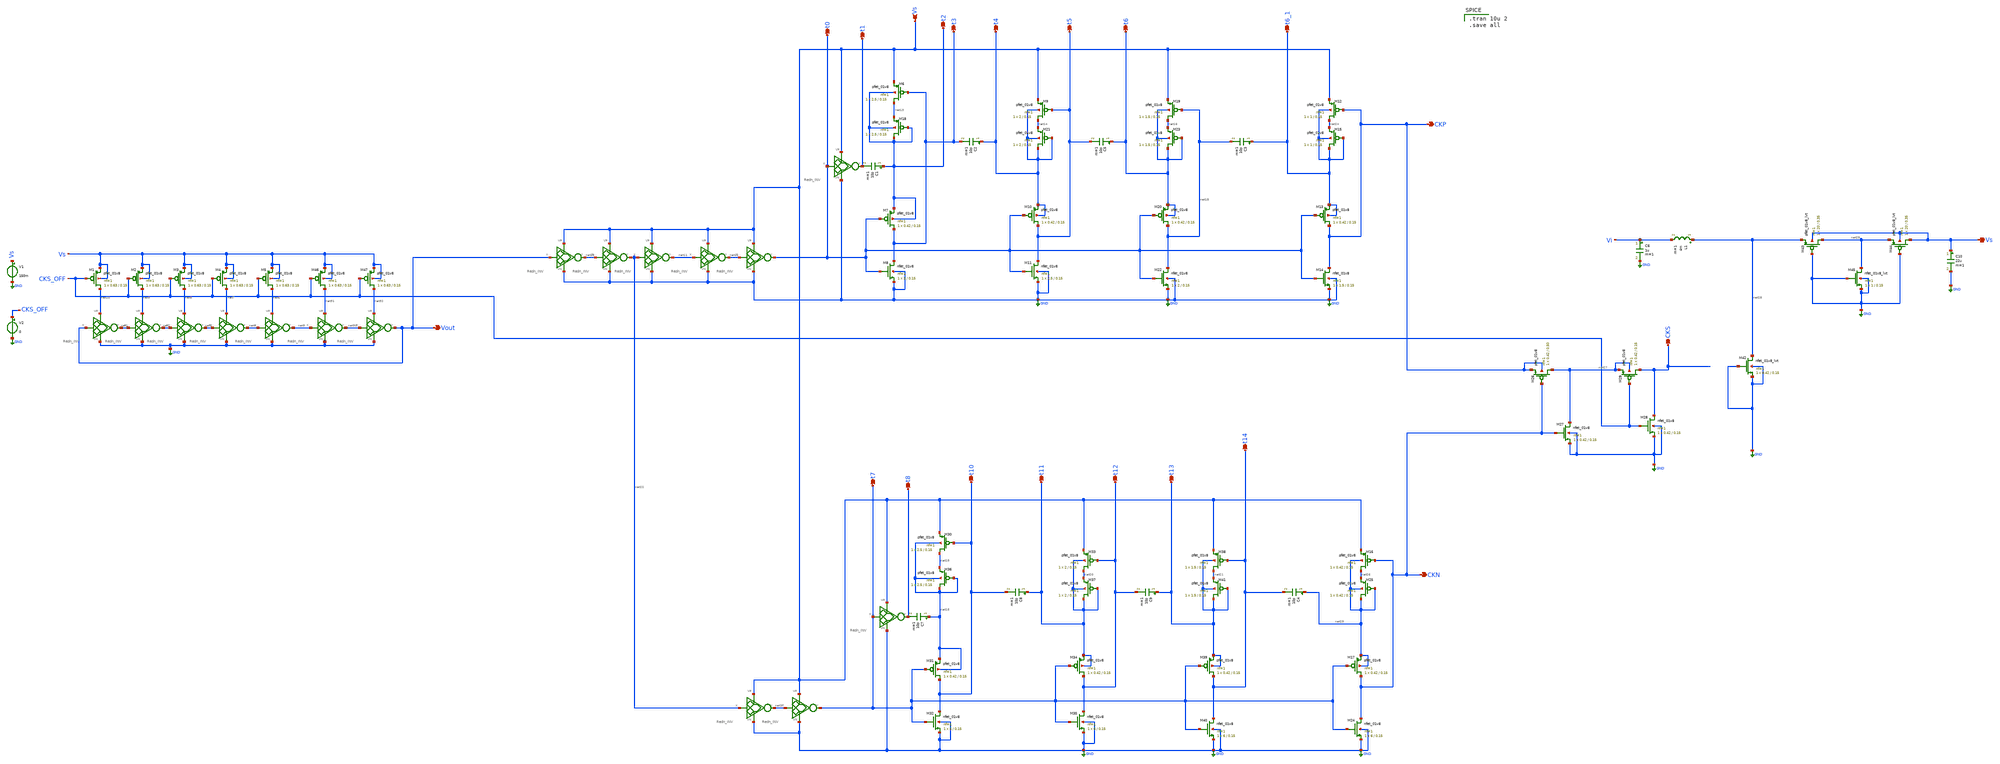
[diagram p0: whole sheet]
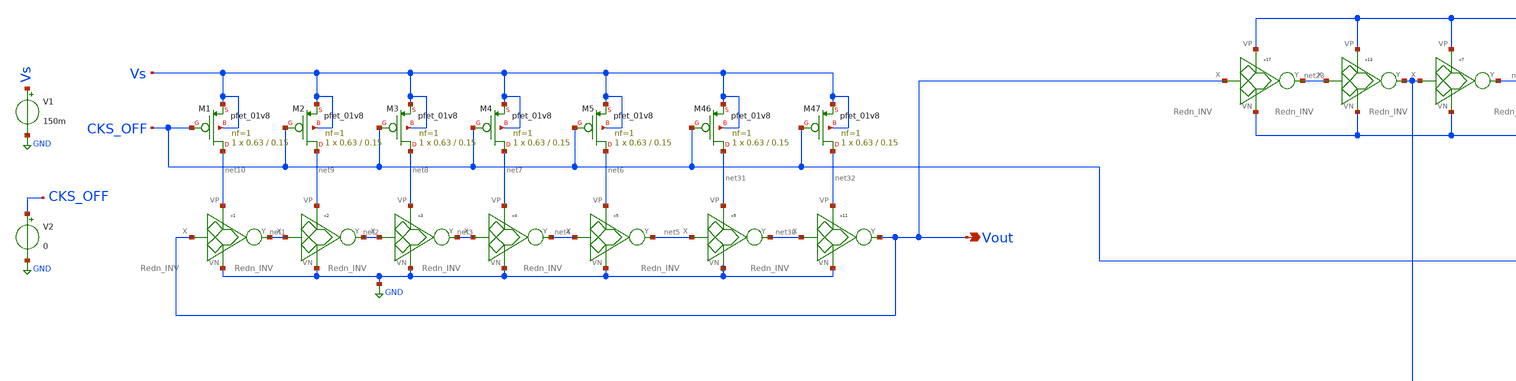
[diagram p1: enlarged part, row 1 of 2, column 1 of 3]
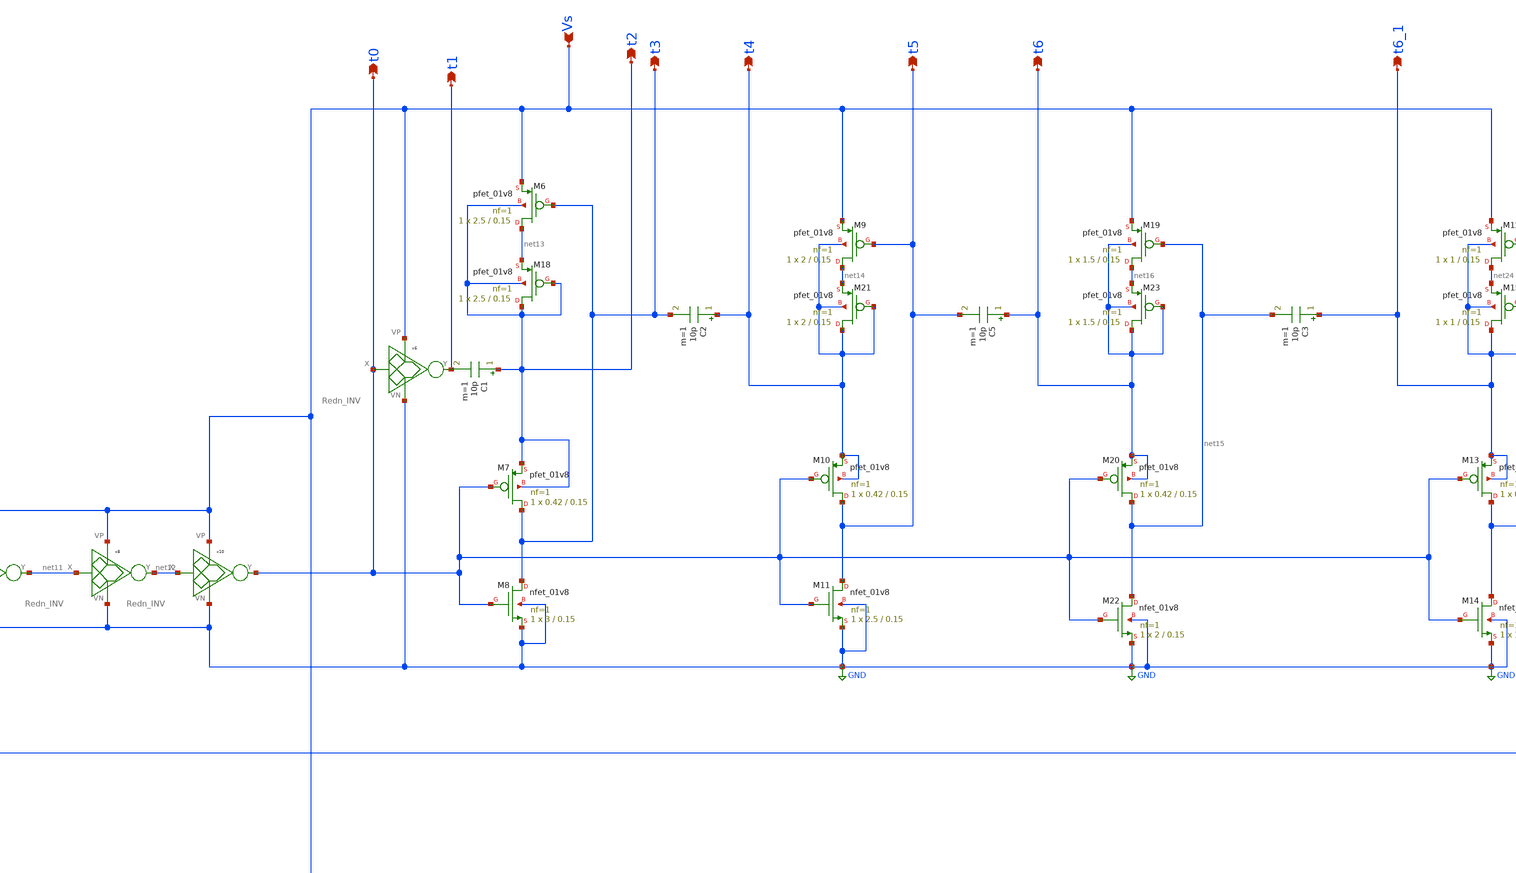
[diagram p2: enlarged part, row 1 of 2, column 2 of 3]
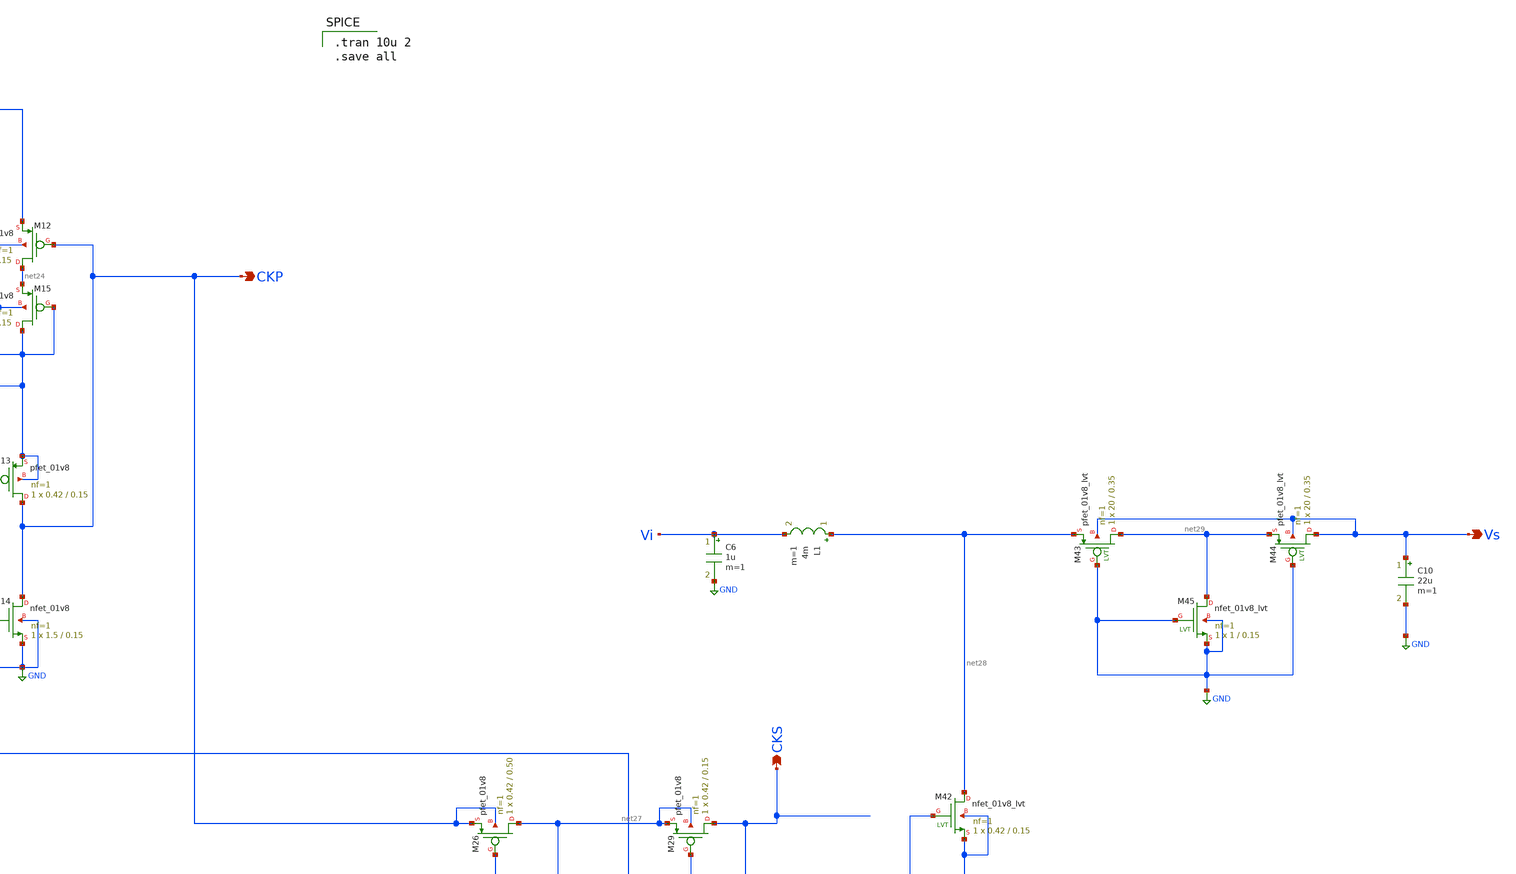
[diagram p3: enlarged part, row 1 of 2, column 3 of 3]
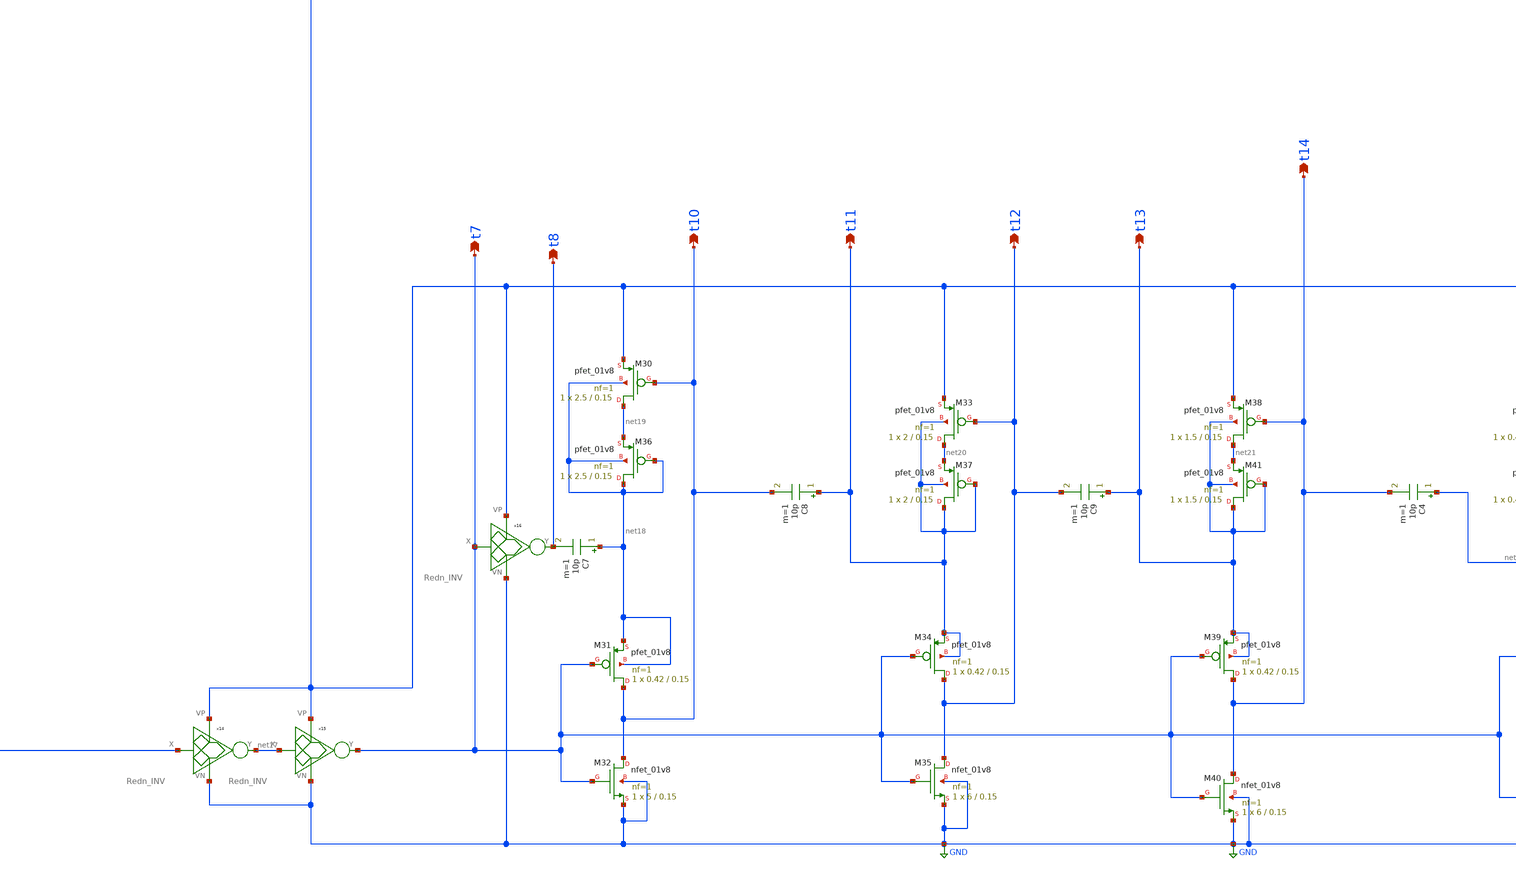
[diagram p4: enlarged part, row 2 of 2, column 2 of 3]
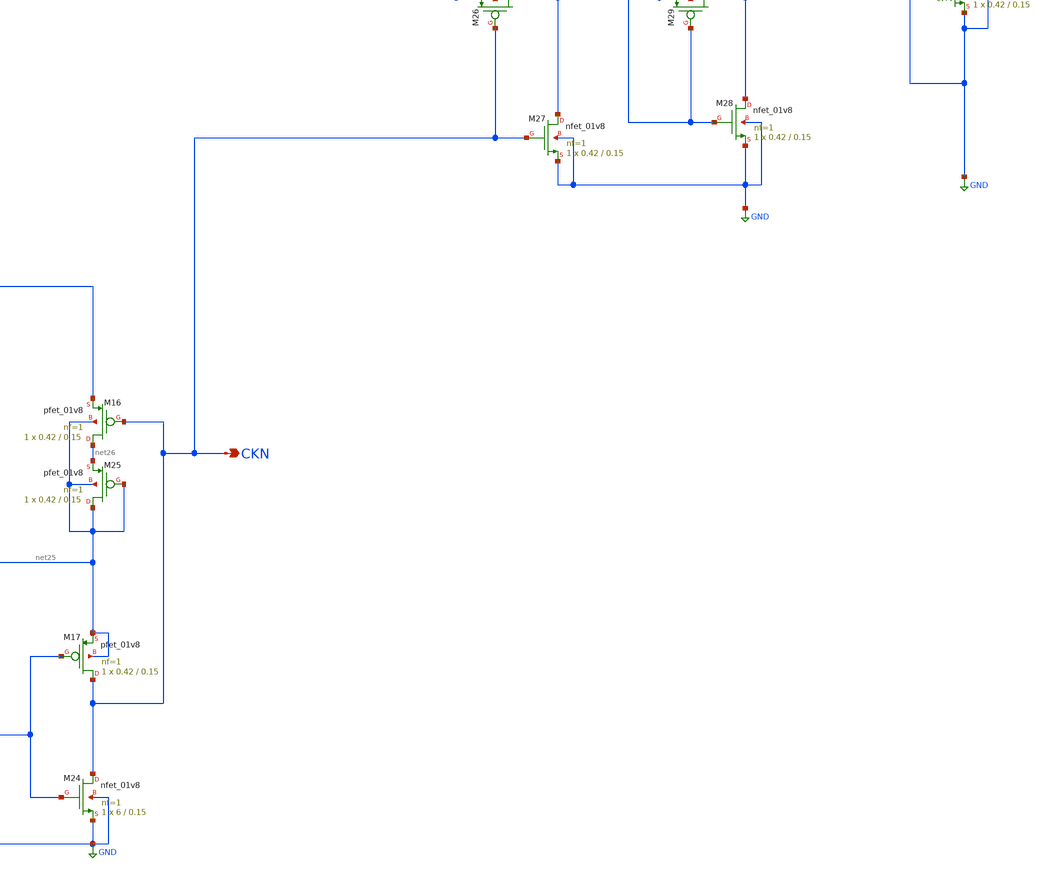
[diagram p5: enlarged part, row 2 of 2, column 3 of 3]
** sch_path: Blocks/Startup Converter/Startup_Cnv_2.sch
**.subckt Startup_Cnv_2 Vout Vs t2 t3 t4 t1 t0 t6 t5 t10 t11 t8 t7 t13 t12 CKP t6_1 CKN t14 CKS Vs
*.opin Vout
*.ipin Vs
*.opin t2
*.opin t3
*.opin t4
*.opin t1
*.opin t0
*.opin t6
*.opin t5
*.opin t10
*.opin t11
*.opin t8
*.opin t7
*.opin t13
*.opin t12
*.opin CKP
*.opin t6_1
*.opin CKN
*.opin t14
*.opin CKS
*.opin Vs
V1 Vs GND 150m
XM1 net10 CKS_OFF Vs Vs sky130_fd_pr__pfet_01v8 L=0.15 W=0.63 nf=1 ad='int((nf+1)/2) * W/nf * 0.29' as='int((nf+2)/2) * W/nf * 0.29'
+ pd='2*int((nf+1)/2) * (W/nf + 0.29)' ps='2*int((nf+2)/2) * (W/nf + 0.29)' nrd='0.29 / W' nrs='0.29 / W'
+ sa=0 sb=0 sd=0 mult=1 m=1
XM2 net9 CKS_OFF Vs Vs sky130_fd_pr__pfet_01v8 L=0.15 W=0.63 nf=1 ad='int((nf+1)/2) * W/nf * 0.29' as='int((nf+2)/2) * W/nf * 0.29'
+ pd='2*int((nf+1)/2) * (W/nf + 0.29)' ps='2*int((nf+2)/2) * (W/nf + 0.29)' nrd='0.29 / W' nrs='0.29 / W'
+ sa=0 sb=0 sd=0 mult=1 m=1
XM3 net8 CKS_OFF Vs Vs sky130_fd_pr__pfet_01v8 L=0.15 W=0.63 nf=1 ad='int((nf+1)/2) * W/nf * 0.29' as='int((nf+2)/2) * W/nf * 0.29'
+ pd='2*int((nf+1)/2) * (W/nf + 0.29)' ps='2*int((nf+2)/2) * (W/nf + 0.29)' nrd='0.29 / W' nrs='0.29 / W'
+ sa=0 sb=0 sd=0 mult=1 m=1
XM4 net7 CKS_OFF Vs Vs sky130_fd_pr__pfet_01v8 L=0.15 W=0.63 nf=1 ad='int((nf+1)/2) * W/nf * 0.29' as='int((nf+2)/2) * W/nf * 0.29'
+ pd='2*int((nf+1)/2) * (W/nf + 0.29)' ps='2*int((nf+2)/2) * (W/nf + 0.29)' nrd='0.29 / W' nrs='0.29 / W'
+ sa=0 sb=0 sd=0 mult=1 m=1
XM5 net6 CKS_OFF Vs Vs sky130_fd_pr__pfet_01v8 L=0.15 W=0.63 nf=1 ad='int((nf+1)/2) * W/nf * 0.29' as='int((nf+2)/2) * W/nf * 0.29'
+ pd='2*int((nf+1)/2) * (W/nf + 0.29)' ps='2*int((nf+2)/2) * (W/nf + 0.29)' nrd='0.29 / W' nrs='0.29 / W'
+ sa=0 sb=0 sd=0 mult=1 m=1
V2 CKS_OFF GND 0
x1 Vout net1 net10 GND Redn_INV
x2 net1 net2 net9 GND Redn_INV
x3 net2 net3 net8 GND Redn_INV
x4 net3 net4 net7 GND Redn_INV
x5 net4 net5 net6 GND Redn_INV
C1 t2 t1 10p m=1
XM6 net13 t3 Vs t2 sky130_fd_pr__pfet_01v8 L=0.15 W=2.5 nf=1 ad='int((nf+1)/2) * W/nf * 0.29' as='int((nf+2)/2) * W/nf * 0.29'
+ pd='2*int((nf+1)/2) * (W/nf + 0.29)' ps='2*int((nf+2)/2) * (W/nf + 0.29)' nrd='0.29 / W' nrs='0.29 / W'
+ sa=0 sb=0 sd=0 mult=1 m=1
XM7 t3 t0 t2 t2 sky130_fd_pr__pfet_01v8 L=0.15 W=0.42 nf=1 ad='int((nf+1)/2) * W/nf * 0.29' as='int((nf+2)/2) * W/nf * 0.29'
+ pd='2*int((nf+1)/2) * (W/nf + 0.29)' ps='2*int((nf+2)/2) * (W/nf + 0.29)' nrd='0.29 / W' nrs='0.29 / W'
+ sa=0 sb=0 sd=0 mult=1 m=1
XM8 t3 t0 GND GND sky130_fd_pr__nfet_01v8 L=0.15 W=3 nf=1 ad='int((nf+1)/2) * W/nf * 0.29' as='int((nf+2)/2) * W/nf * 0.29'
+ pd='2*int((nf+1)/2) * (W/nf + 0.29)' ps='2*int((nf+2)/2) * (W/nf + 0.29)' nrd='0.29 / W' nrs='0.29 / W'
+ sa=0 sb=0 sd=0 mult=1 m=1
XM9 net14 t5 Vs t4 sky130_fd_pr__pfet_01v8 L=0.15 W=2 nf=1 ad='int((nf+1)/2) * W/nf * 0.29' as='int((nf+2)/2) * W/nf * 0.29'
+ pd='2*int((nf+1)/2) * (W/nf + 0.29)' ps='2*int((nf+2)/2) * (W/nf + 0.29)' nrd='0.29 / W' nrs='0.29 / W'
+ sa=0 sb=0 sd=0 mult=1 m=1
XM10 t5 t0 t4 t4 sky130_fd_pr__pfet_01v8 L=0.15 W=0.42 nf=1 ad='int((nf+1)/2) * W/nf * 0.29' as='int((nf+2)/2) * W/nf * 0.29'
+ pd='2*int((nf+1)/2) * (W/nf + 0.29)' ps='2*int((nf+2)/2) * (W/nf + 0.29)' nrd='0.29 / W' nrs='0.29 / W'
+ sa=0 sb=0 sd=0 mult=1 m=1
XM11 t5 t0 GND GND sky130_fd_pr__nfet_01v8 L=0.15 W=2.5 nf=1 ad='int((nf+1)/2) * W/nf * 0.29' as='int((nf+2)/2) * W/nf * 0.29'
+ pd='2*int((nf+1)/2) * (W/nf + 0.29)' ps='2*int((nf+2)/2) * (W/nf + 0.29)' nrd='0.29 / W' nrs='0.29 / W'
+ sa=0 sb=0 sd=0 mult=1 m=1
XM18 t2 t2 net13 t2 sky130_fd_pr__pfet_01v8 L=0.15 W=2.5 nf=1 ad='int((nf+1)/2) * W/nf * 0.29' as='int((nf+2)/2) * W/nf * 0.29'
+ pd='2*int((nf+1)/2) * (W/nf + 0.29)' ps='2*int((nf+2)/2) * (W/nf + 0.29)' nrd='0.29 / W' nrs='0.29 / W'
+ sa=0 sb=0 sd=0 mult=1 m=1
XM21 t4 t4 net14 t4 sky130_fd_pr__pfet_01v8 L=0.15 W=2 nf=1 ad='int((nf+1)/2) * W/nf * 0.29' as='int((nf+2)/2) * W/nf * 0.29'
+ pd='2*int((nf+1)/2) * (W/nf + 0.29)' ps='2*int((nf+2)/2) * (W/nf + 0.29)' nrd='0.29 / W' nrs='0.29 / W'
+ sa=0 sb=0 sd=0 mult=1 m=1
C2 t4 t3 10p m=1
x7 net22 net11 Vs GND Redn_INV
x8 net11 net12 Vs GND Redn_INV
x10 net12 t0 Vs GND Redn_INV
x6 t0 t1 Vs GND Redn_INV
XM19 net16 net15 Vs t6 sky130_fd_pr__pfet_01v8 L=0.15 W=1.5 nf=1 ad='int((nf+1)/2) * W/nf * 0.29' as='int((nf+2)/2) * W/nf * 0.29'
+ pd='2*int((nf+1)/2) * (W/nf + 0.29)' ps='2*int((nf+2)/2) * (W/nf + 0.29)' nrd='0.29 / W' nrs='0.29 / W'
+ sa=0 sb=0 sd=0 mult=1 m=1
XM20 net15 t0 t6 t6 sky130_fd_pr__pfet_01v8 L=0.15 W=0.42 nf=1 ad='int((nf+1)/2) * W/nf * 0.29' as='int((nf+2)/2) * W/nf * 0.29'
+ pd='2*int((nf+1)/2) * (W/nf + 0.29)' ps='2*int((nf+2)/2) * (W/nf + 0.29)' nrd='0.29 / W' nrs='0.29 / W'
+ sa=0 sb=0 sd=0 mult=1 m=1
XM22 net15 t0 GND GND sky130_fd_pr__nfet_01v8 L=0.15 W=2 nf=1 ad='int((nf+1)/2) * W/nf * 0.29' as='int((nf+2)/2) * W/nf * 0.29'
+ pd='2*int((nf+1)/2) * (W/nf + 0.29)' ps='2*int((nf+2)/2) * (W/nf + 0.29)' nrd='0.29 / W' nrs='0.29 / W'
+ sa=0 sb=0 sd=0 mult=1 m=1
XM23 t6 t6 net16 t6 sky130_fd_pr__pfet_01v8 L=0.15 W=1.5 nf=1 ad='int((nf+1)/2) * W/nf * 0.29' as='int((nf+2)/2) * W/nf * 0.29'
+ pd='2*int((nf+1)/2) * (W/nf + 0.29)' ps='2*int((nf+2)/2) * (W/nf + 0.29)' nrd='0.29 / W' nrs='0.29 / W'
+ sa=0 sb=0 sd=0 mult=1 m=1
C5 t6 t5 10p m=1
C7 net18 t8 10p m=1
XM30 net19 t10 Vs net18 sky130_fd_pr__pfet_01v8 L=0.15 W=2.5 nf=1 ad='int((nf+1)/2) * W/nf * 0.29' as='int((nf+2)/2) * W/nf * 0.29'
+ pd='2*int((nf+1)/2) * (W/nf + 0.29)' ps='2*int((nf+2)/2) * (W/nf + 0.29)' nrd='0.29 / W' nrs='0.29 / W'
+ sa=0 sb=0 sd=0 mult=1 m=1
XM31 t10 t7 net18 net18 sky130_fd_pr__pfet_01v8 L=0.15 W=0.42 nf=1 ad='int((nf+1)/2) * W/nf * 0.29' as='int((nf+2)/2) * W/nf * 0.29'
+ pd='2*int((nf+1)/2) * (W/nf + 0.29)' ps='2*int((nf+2)/2) * (W/nf + 0.29)' nrd='0.29 / W' nrs='0.29 / W'
+ sa=0 sb=0 sd=0 mult=1 m=1
XM32 t10 t7 GND GND sky130_fd_pr__nfet_01v8 L=0.15 W=5 nf=1 ad='int((nf+1)/2) * W/nf * 0.29' as='int((nf+2)/2) * W/nf * 0.29'
+ pd='2*int((nf+1)/2) * (W/nf + 0.29)' ps='2*int((nf+2)/2) * (W/nf + 0.29)' nrd='0.29 / W' nrs='0.29 / W'
+ sa=0 sb=0 sd=0 mult=1 m=1
XM33 net20 t12 Vs t11 sky130_fd_pr__pfet_01v8 L=0.15 W=2 nf=1 ad='int((nf+1)/2) * W/nf * 0.29' as='int((nf+2)/2) * W/nf * 0.29'
+ pd='2*int((nf+1)/2) * (W/nf + 0.29)' ps='2*int((nf+2)/2) * (W/nf + 0.29)' nrd='0.29 / W' nrs='0.29 / W'
+ sa=0 sb=0 sd=0 mult=1 m=1
XM34 t12 t7 t11 t11 sky130_fd_pr__pfet_01v8 L=0.15 W=0.42 nf=1 ad='int((nf+1)/2) * W/nf * 0.29' as='int((nf+2)/2) * W/nf * 0.29'
+ pd='2*int((nf+1)/2) * (W/nf + 0.29)' ps='2*int((nf+2)/2) * (W/nf + 0.29)' nrd='0.29 / W' nrs='0.29 / W'
+ sa=0 sb=0 sd=0 mult=1 m=1
XM35 t12 t7 GND GND sky130_fd_pr__nfet_01v8 L=0.15 W=6 nf=1 ad='int((nf+1)/2) * W/nf * 0.29' as='int((nf+2)/2) * W/nf * 0.29'
+ pd='2*int((nf+1)/2) * (W/nf + 0.29)' ps='2*int((nf+2)/2) * (W/nf + 0.29)' nrd='0.29 / W' nrs='0.29 / W'
+ sa=0 sb=0 sd=0 mult=1 m=1
XM36 net18 net18 net19 net18 sky130_fd_pr__pfet_01v8 L=0.15 W=2.5 nf=1 ad='int((nf+1)/2) * W/nf * 0.29'
+ as='int((nf+2)/2) * W/nf * 0.29' pd='2*int((nf+1)/2) * (W/nf + 0.29)' ps='2*int((nf+2)/2) * (W/nf + 0.29)'
+ nrd='0.29 / W' nrs='0.29 / W' sa=0 sb=0 sd=0 mult=1 m=1
XM37 t11 t11 net20 t11 sky130_fd_pr__pfet_01v8 L=0.15 W=2 nf=1 ad='int((nf+1)/2) * W/nf * 0.29' as='int((nf+2)/2) * W/nf * 0.29'
+ pd='2*int((nf+1)/2) * (W/nf + 0.29)' ps='2*int((nf+2)/2) * (W/nf + 0.29)' nrd='0.29 / W' nrs='0.29 / W'
+ sa=0 sb=0 sd=0 mult=1 m=1
C8 t11 t10 10p m=1
x14 net22 net17 Vs GND Redn_INV
x15 net17 t7 Vs GND Redn_INV
x16 t7 t8 Vs GND Redn_INV
XM38 net21 t14 Vs t13 sky130_fd_pr__pfet_01v8 L=0.15 W=1.5 nf=1 ad='int((nf+1)/2) * W/nf * 0.29' as='int((nf+2)/2) * W/nf * 0.29'
+ pd='2*int((nf+1)/2) * (W/nf + 0.29)' ps='2*int((nf+2)/2) * (W/nf + 0.29)' nrd='0.29 / W' nrs='0.29 / W'
+ sa=0 sb=0 sd=0 mult=1 m=1
XM39 t14 t7 t13 t13 sky130_fd_pr__pfet_01v8 L=0.15 W=0.42 nf=1 ad='int((nf+1)/2) * W/nf * 0.29' as='int((nf+2)/2) * W/nf * 0.29'
+ pd='2*int((nf+1)/2) * (W/nf + 0.29)' ps='2*int((nf+2)/2) * (W/nf + 0.29)' nrd='0.29 / W' nrs='0.29 / W'
+ sa=0 sb=0 sd=0 mult=1 m=1
XM40 t14 t7 GND GND sky130_fd_pr__nfet_01v8 L=0.15 W=6 nf=1 ad='int((nf+1)/2) * W/nf * 0.29' as='int((nf+2)/2) * W/nf * 0.29'
+ pd='2*int((nf+1)/2) * (W/nf + 0.29)' ps='2*int((nf+2)/2) * (W/nf + 0.29)' nrd='0.29 / W' nrs='0.29 / W'
+ sa=0 sb=0 sd=0 mult=1 m=1
XM41 t13 t13 net21 t13 sky130_fd_pr__pfet_01v8 L=0.15 W=1.5 nf=1 ad='int((nf+1)/2) * W/nf * 0.29' as='int((nf+2)/2) * W/nf * 0.29'
+ pd='2*int((nf+1)/2) * (W/nf + 0.29)' ps='2*int((nf+2)/2) * (W/nf + 0.29)' nrd='0.29 / W' nrs='0.29 / W'
+ sa=0 sb=0 sd=0 mult=1 m=1
C9 t13 t12 10p m=1
x13 net23 net22 Vs GND Redn_INV
x17 Vout net23 Vs GND Redn_INV
XM12 net24 CKP Vs t6_1 sky130_fd_pr__pfet_01v8 L=0.15 W=1 nf=1 ad='int((nf+1)/2) * W/nf * 0.29' as='int((nf+2)/2) * W/nf * 0.29'
+ pd='2*int((nf+1)/2) * (W/nf + 0.29)' ps='2*int((nf+2)/2) * (W/nf + 0.29)' nrd='0.29 / W' nrs='0.29 / W'
+ sa=0 sb=0 sd=0 mult=1 m=1
XM13 CKP t0 t6_1 t6_1 sky130_fd_pr__pfet_01v8 L=0.15 W=0.42 nf=1 ad='int((nf+1)/2) * W/nf * 0.29' as='int((nf+2)/2) * W/nf * 0.29'
+ pd='2*int((nf+1)/2) * (W/nf + 0.29)' ps='2*int((nf+2)/2) * (W/nf + 0.29)' nrd='0.29 / W' nrs='0.29 / W'
+ sa=0 sb=0 sd=0 mult=1 m=1
XM14 CKP t0 GND GND sky130_fd_pr__nfet_01v8 L=0.15 W=1.5 nf=1 ad='int((nf+1)/2) * W/nf * 0.29' as='int((nf+2)/2) * W/nf * 0.29'
+ pd='2*int((nf+1)/2) * (W/nf + 0.29)' ps='2*int((nf+2)/2) * (W/nf + 0.29)' nrd='0.29 / W' nrs='0.29 / W'
+ sa=0 sb=0 sd=0 mult=1 m=1
XM15 t6_1 t6_1 net24 t6_1 sky130_fd_pr__pfet_01v8 L=0.15 W=1 nf=1 ad='int((nf+1)/2) * W/nf * 0.29' as='int((nf+2)/2) * W/nf * 0.29'
+ pd='2*int((nf+1)/2) * (W/nf + 0.29)' ps='2*int((nf+2)/2) * (W/nf + 0.29)' nrd='0.29 / W' nrs='0.29 / W'
+ sa=0 sb=0 sd=0 mult=1 m=1
C3 t6_1 net15 10p m=1
XM16 net26 CKN Vs net25 sky130_fd_pr__pfet_01v8 L=0.15 W=0.42 nf=1 ad='int((nf+1)/2) * W/nf * 0.29' as='int((nf+2)/2) * W/nf * 0.29'
+ pd='2*int((nf+1)/2) * (W/nf + 0.29)' ps='2*int((nf+2)/2) * (W/nf + 0.29)' nrd='0.29 / W' nrs='0.29 / W'
+ sa=0 sb=0 sd=0 mult=1 m=1
XM17 CKN t7 net25 net25 sky130_fd_pr__pfet_01v8 L=0.15 W=0.42 nf=1 ad='int((nf+1)/2) * W/nf * 0.29' as='int((nf+2)/2) * W/nf * 0.29'
+ pd='2*int((nf+1)/2) * (W/nf + 0.29)' ps='2*int((nf+2)/2) * (W/nf + 0.29)' nrd='0.29 / W' nrs='0.29 / W'
+ sa=0 sb=0 sd=0 mult=1 m=1
XM24 CKN t7 GND GND sky130_fd_pr__nfet_01v8 L=0.15 W=6 nf=1 ad='int((nf+1)/2) * W/nf * 0.29' as='int((nf+2)/2) * W/nf * 0.29'
+ pd='2*int((nf+1)/2) * (W/nf + 0.29)' ps='2*int((nf+2)/2) * (W/nf + 0.29)' nrd='0.29 / W' nrs='0.29 / W'
+ sa=0 sb=0 sd=0 mult=1 m=1
XM25 net25 net25 net26 net25 sky130_fd_pr__pfet_01v8 L=0.15 W=0.42 nf=1 ad='int((nf+1)/2) * W/nf * 0.29'
+ as='int((nf+2)/2) * W/nf * 0.29' pd='2*int((nf+1)/2) * (W/nf + 0.29)' ps='2*int((nf+2)/2) * (W/nf + 0.29)'
+ nrd='0.29 / W' nrs='0.29 / W' sa=0 sb=0 sd=0 mult=1 m=1
C4 net25 t14 10p m=1
XM26 net27 CKN CKP CKP sky130_fd_pr__pfet_01v8 L=0.50 W=0.42 nf=1 ad='int((nf+1)/2) * W/nf * 0.29' as='int((nf+2)/2) * W/nf * 0.29'
+ pd='2*int((nf+1)/2) * (W/nf + 0.29)' ps='2*int((nf+2)/2) * (W/nf + 0.29)' nrd='0.29 / W' nrs='0.29 / W'
+ sa=0 sb=0 sd=0 mult=1 m=1
XM27 net27 CKN GND GND sky130_fd_pr__nfet_01v8 L=0.15 W=0.42 nf=1 ad='int((nf+1)/2) * W/nf * 0.29' as='int((nf+2)/2) * W/nf * 0.29'
+ pd='2*int((nf+1)/2) * (W/nf + 0.29)' ps='2*int((nf+2)/2) * (W/nf + 0.29)' nrd='0.29 / W' nrs='0.29 / W'
+ sa=0 sb=0 sd=0 mult=1 m=1
XM28 CKS CKS_OFF GND GND sky130_fd_pr__nfet_01v8 L=0.15 W=0.42 nf=1 ad='int((nf+1)/2) * W/nf * 0.29'
+ as='int((nf+2)/2) * W/nf * 0.29' pd='2*int((nf+1)/2) * (W/nf + 0.29)' ps='2*int((nf+2)/2) * (W/nf + 0.29)'
+ nrd='0.29 / W' nrs='0.29 / W' sa=0 sb=0 sd=0 mult=1 m=1
XM29 CKS CKS_OFF net27 net27 sky130_fd_pr__pfet_01v8 L=0.15 W=0.42 nf=1 ad='int((nf+1)/2) * W/nf * 0.29'
+ as='int((nf+2)/2) * W/nf * 0.29' pd='2*int((nf+1)/2) * (W/nf + 0.29)' ps='2*int((nf+2)/2) * (W/nf + 0.29)'
+ nrd='0.29 / W' nrs='0.29 / W' sa=0 sb=0 sd=0 mult=1 m=1
C6 Vi GND 1u m=1
L1 net28 Vi 4m m=1
C10 Vs GND 22u m=1
XM42 net28 GND GND GND sky130_fd_pr__nfet_01v8_lvt L=0.15 W=0.42 nf=1 ad='int((nf+1)/2) * W/nf * 0.29'
+ as='int((nf+2)/2) * W/nf * 0.29' pd='2*int((nf+1)/2) * (W/nf + 0.29)' ps='2*int((nf+2)/2) * (W/nf + 0.29)'
+ nrd='0.29 / W' nrs='0.29 / W' sa=0 sb=0 sd=0 mult=1 m=1
XM43 net29 GND net28 Vs sky130_fd_pr__pfet_01v8_lvt L=0.35 W=20 nf=1 ad='int((nf+1)/2) * W/nf * 0.29'
+ as='int((nf+2)/2) * W/nf * 0.29' pd='2*int((nf+1)/2) * (W/nf + 0.29)' ps='2*int((nf+2)/2) * (W/nf + 0.29)'
+ nrd='0.29 / W' nrs='0.29 / W' sa=0 sb=0 sd=0 mult=1 m=1
XM44 Vs GND net29 Vs sky130_fd_pr__pfet_01v8_lvt L=0.35 W=20 nf=1 ad='int((nf+1)/2) * W/nf * 0.29' as='int((nf+2)/2) * W/nf * 0.29'
+ pd='2*int((nf+1)/2) * (W/nf + 0.29)' ps='2*int((nf+2)/2) * (W/nf + 0.29)' nrd='0.29 / W' nrs='0.29 / W'
+ sa=0 sb=0 sd=0 mult=1 m=1
XM45 net29 GND GND GND sky130_fd_pr__nfet_01v8_lvt L=0.15 W=1 nf=1 ad='int((nf+1)/2) * W/nf * 0.29' as='int((nf+2)/2) * W/nf * 0.29'
+ pd='2*int((nf+1)/2) * (W/nf + 0.29)' ps='2*int((nf+2)/2) * (W/nf + 0.29)' nrd='0.29 / W' nrs='0.29 / W'
+ sa=0 sb=0 sd=0 mult=1 m=1
x9 net5 net30 net31 GND Redn_INV
x11 net30 Vout net32 GND Redn_INV
XM46 net31 CKS_OFF Vs Vs sky130_fd_pr__pfet_01v8 L=0.15 W=0.63 nf=1 ad='int((nf+1)/2) * W/nf * 0.29'
+ as='int((nf+2)/2) * W/nf * 0.29' pd='2*int((nf+1)/2) * (W/nf + 0.29)' ps='2*int((nf+2)/2) * (W/nf + 0.29)'
+ nrd='0.29 / W' nrs='0.29 / W' sa=0 sb=0 sd=0 mult=1 m=1
XM47 net32 CKS_OFF Vs Vs sky130_fd_pr__pfet_01v8 L=0.15 W=0.63 nf=1 ad='int((nf+1)/2) * W/nf * 0.29'
+ as='int((nf+2)/2) * W/nf * 0.29' pd='2*int((nf+1)/2) * (W/nf + 0.29)' ps='2*int((nf+2)/2) * (W/nf + 0.29)'
+ nrd='0.29 / W' nrs='0.29 / W' sa=0 sb=0 sd=0 mult=1 m=1
**** begin user architecture code

** opencircuitdesign pdks install
.lib $::SKYWATER_MODELS/sky130.lib.spice tt



.tran 10u 2
.save all

**** end user architecture code
**.ends

* expanding   symbol:  component/Reduntant_Inverter/Redn_INV.sym # of pins=4
** sym_path: component/Reduntant_Inverter/Redn_INV.sym
** sch_path: component/Reduntant_Inverter/Redn_INV.sch
.subckt Redn_INV X Y VP VN
*.opin Y
*.ipin X
*.iopin VP
*.iopin VN
XM15 net4 X VN VN sky130_fd_pr__nfet_01v8_lvt L=0.15 W=1 nf=1 ad='int((nf+1)/2) * W/nf * 0.29' as='int((nf+2)/2) * W/nf * 0.29'
+ pd='2*int((nf+1)/2) * (W/nf + 0.29)' ps='2*int((nf+2)/2) * (W/nf + 0.29)' nrd='0.29 / W' nrs='0.29 / W'
+ sa=0 sb=0 sd=0 mult=1 m=1
XM1 net5 X net3 VN sky130_fd_pr__nfet_01v8_lvt L=0.15 W=3.25 nf=1 ad='int((nf+1)/2) * W/nf * 0.29' as='int((nf+2)/2) * W/nf * 0.29'
+ pd='2*int((nf+1)/2) * (W/nf + 0.29)' ps='2*int((nf+2)/2) * (W/nf + 0.29)' nrd='0.29 / W' nrs='0.29 / W'
+ sa=0 sb=0 sd=0 mult=1 m=1
XM16 Y X net6 VN sky130_fd_pr__nfet_01v8_lvt L=0.15 W=6.5 nf=1 ad='int((nf+1)/2) * W/nf * 0.29' as='int((nf+2)/2) * W/nf * 0.29'
+ pd='2*int((nf+1)/2) * (W/nf + 0.29)' ps='2*int((nf+2)/2) * (W/nf + 0.29)' nrd='0.29 / W' nrs='0.29 / W'
+ sa=0 sb=0 sd=0 mult=1 m=1
XM17 net3 X VN VN sky130_fd_pr__nfet_01v8_lvt L=0.15 W=3.25 nf=1 ad='int((nf+1)/2) * W/nf * 0.29' as='int((nf+2)/2) * W/nf * 0.29'
+ pd='2*int((nf+1)/2) * (W/nf + 0.29)' ps='2*int((nf+2)/2) * (W/nf + 0.29)' nrd='0.29 / W' nrs='0.29 / W'
+ sa=0 sb=0 sd=0 mult=1 m=1
XM18 net2 X VN VN sky130_fd_pr__nfet_01v8_lvt L=0.15 W=1.5 nf=1 ad='int((nf+1)/2) * W/nf * 0.29' as='int((nf+2)/2) * W/nf * 0.29'
+ pd='2*int((nf+1)/2) * (W/nf + 0.29)' ps='2*int((nf+2)/2) * (W/nf + 0.29)' nrd='0.29 / W' nrs='0.29 / W'
+ sa=0 sb=0 sd=0 mult=1 m=1
XM19 net1 X VN VN sky130_fd_pr__nfet_01v8_lvt L=0.15 W=6.5 nf=1 ad='int((nf+1)/2) * W/nf * 0.29' as='int((nf+2)/2) * W/nf * 0.29'
+ pd='2*int((nf+1)/2) * (W/nf + 0.29)' ps='2*int((nf+2)/2) * (W/nf + 0.29)' nrd='0.29 / W' nrs='0.29 / W'
+ sa=0 sb=0 sd=0 mult=1 m=1
XM20 net6 X net1 VN sky130_fd_pr__nfet_01v8_lvt L=0.15 W=6.5 nf=1 ad='int((nf+1)/2) * W/nf * 0.29' as='int((nf+2)/2) * W/nf * 0.29'
+ pd='2*int((nf+1)/2) * (W/nf + 0.29)' ps='2*int((nf+2)/2) * (W/nf + 0.29)' nrd='0.29 / W' nrs='0.29 / W'
+ sa=0 sb=0 sd=0 mult=1 m=1
XM2 net4 X VP VP sky130_fd_pr__pfet_01v8 L=0.15 W=10 nf=1 ad='int((nf+1)/2) * W/nf * 0.29' as='int((nf+2)/2) * W/nf * 0.29'
+ pd='2*int((nf+1)/2) * (W/nf + 0.29)' ps='2*int((nf+2)/2) * (W/nf + 0.29)' nrd='0.29 / W' nrs='0.29 / W'
+ sa=0 sb=0 sd=0 mult=1 m=1
XM5 net5 X net4 net4 sky130_fd_pr__pfet_01v8 L=0.15 W=10 nf=1 ad='int((nf+1)/2) * W/nf * 0.29' as='int((nf+2)/2) * W/nf * 0.29'
+ pd='2*int((nf+1)/2) * (W/nf + 0.29)' ps='2*int((nf+2)/2) * (W/nf + 0.29)' nrd='0.29 / W' nrs='0.29 / W'
+ sa=0 sb=0 sd=0 mult=1 m=1
XM6 Y X net5 VP sky130_fd_pr__pfet_01v8 L=0.15 W=10 nf=1 ad='int((nf+1)/2) * W/nf * 0.29' as='int((nf+2)/2) * W/nf * 0.29'
+ pd='2*int((nf+1)/2) * (W/nf + 0.29)' ps='2*int((nf+2)/2) * (W/nf + 0.29)' nrd='0.29 / W' nrs='0.29 / W'
+ sa=0 sb=0 sd=0 mult=1 m=1
XM8 net3 X VP VP sky130_fd_pr__pfet_01v8 L=0.15 W=2 nf=1 ad='int((nf+1)/2) * W/nf * 0.29' as='int((nf+2)/2) * W/nf * 0.29'
+ pd='2*int((nf+1)/2) * (W/nf + 0.29)' ps='2*int((nf+2)/2) * (W/nf + 0.29)' nrd='0.29 / W' nrs='0.29 / W'
+ sa=0 sb=0 sd=0 mult=1 m=1
XM12 net2 X VP VP sky130_fd_pr__pfet_01v8 L=0.15 W=5 nf=1 ad='int((nf+1)/2) * W/nf * 0.29' as='int((nf+2)/2) * W/nf * 0.29'
+ pd='2*int((nf+1)/2) * (W/nf + 0.29)' ps='2*int((nf+2)/2) * (W/nf + 0.29)' nrd='0.29 / W' nrs='0.29 / W'
+ sa=0 sb=0 sd=0 mult=1 m=1
XM14 net6 X net2 VP sky130_fd_pr__pfet_01v8 L=0.15 W=5 nf=1 ad='int((nf+1)/2) * W/nf * 0.29' as='int((nf+2)/2) * W/nf * 0.29'
+ pd='2*int((nf+1)/2) * (W/nf + 0.29)' ps='2*int((nf+2)/2) * (W/nf + 0.29)' nrd='0.29 / W' nrs='0.29 / W'
+ sa=0 sb=0 sd=0 mult=1 m=1
XM21 net1 X VP VP sky130_fd_pr__pfet_01v8 L=0.15 W=1.5 nf=1 ad='int((nf+1)/2) * W/nf * 0.29' as='int((nf+2)/2) * W/nf * 0.29'
+ pd='2*int((nf+1)/2) * (W/nf + 0.29)' ps='2*int((nf+2)/2) * (W/nf + 0.29)' nrd='0.29 / W' nrs='0.29 / W'
+ sa=0 sb=0 sd=0 mult=1 m=1
.ends

.GLOBAL GND
.end
